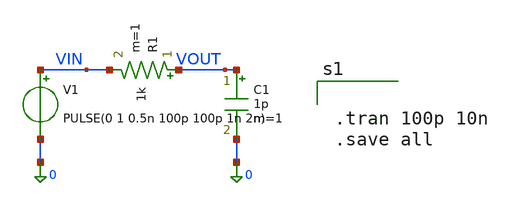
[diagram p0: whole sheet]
** sch_path: designs/luc_testing/rc_circuit_test.sch
**.subckt rc_circuit_test
V1 VIN 0 PULSE(0 1 0.5n 100p 100p 1n 2n)
R1 VOUT VIN 1k m=1
C1 VOUT 0 1p m=1
**** begin user architecture code


.tran 100p 10n
.save all



**** end user architecture code
**.ends
.end
